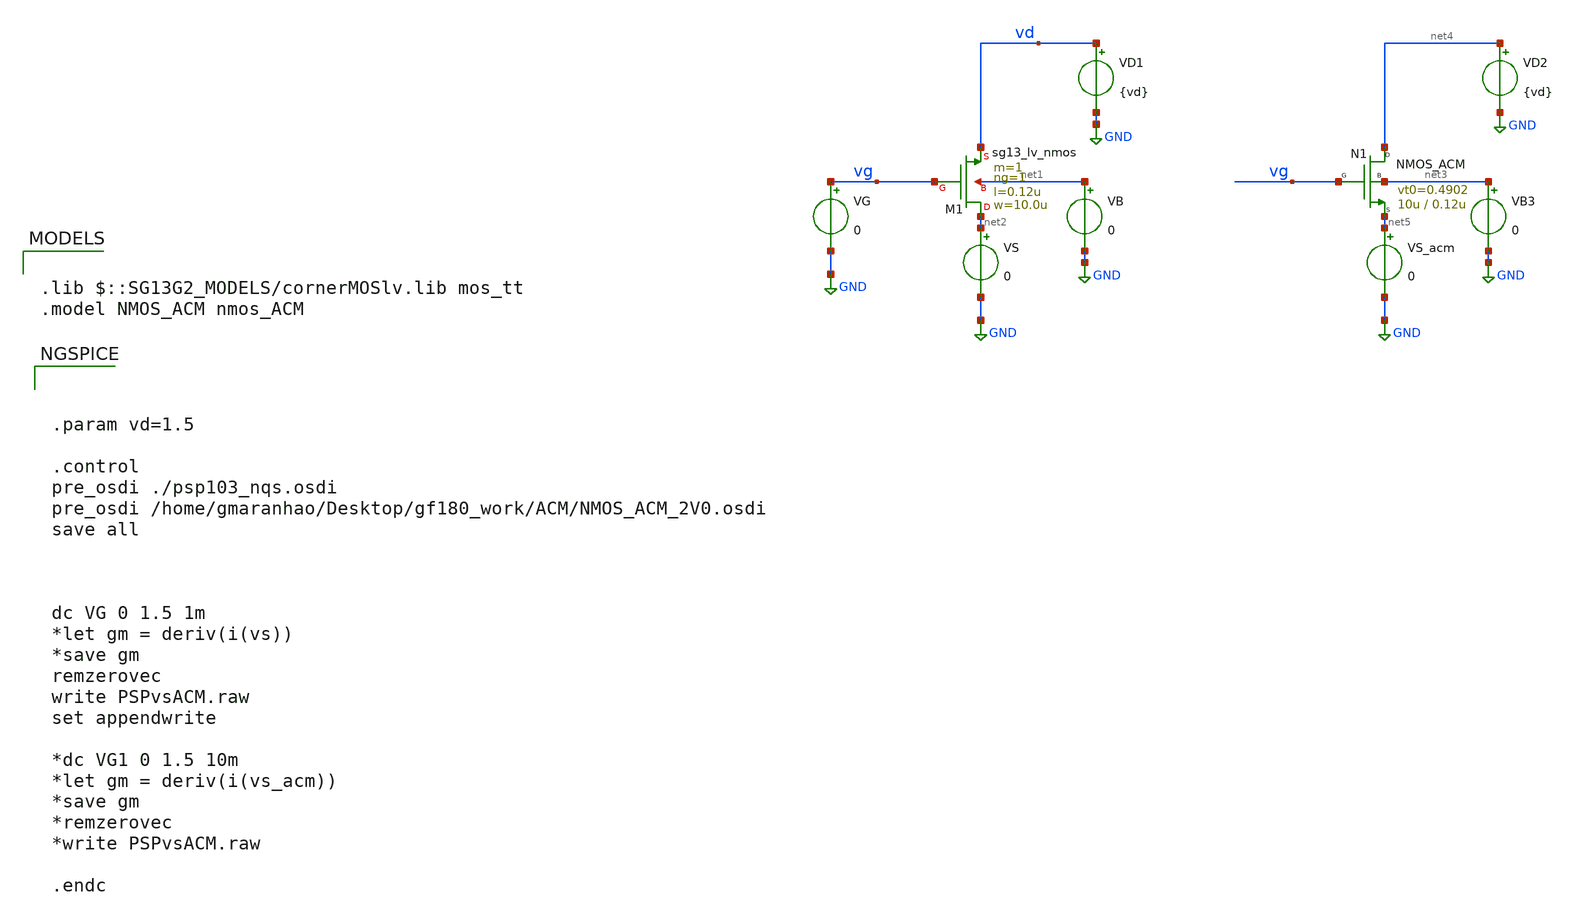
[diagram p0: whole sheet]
** sch_path: ihp_tutorials/PSPvsACM.sch
**.subckt PSPvsACM
VG vg GND 0
VD1 vd GND {vd}
VB net1 GND 0
VS net2 GND 0
N1 net4 vg net5 net3 NMOS_ACM w=10u l=0.12u n=1.414 is=11.77u vt0=0.4902 sigma=53.4m zeta=7m
VB3 net3 GND 0
VS_acm net5 GND 0
VD2 net4 GND {vd}
XM1 net2 vg vd net1 sg13_lv_nmos w=10.0u l=0.12u ng=1 m=1 mm_ok=1
**** begin user architecture code



.param vd=1.5

.control
pre_osdi ./psp103_nqs.osdi
pre_osdi /home/gmaranhao/Desktop/gf180_work/ACM/NMOS_ACM_2V0.osdi
save all



dc VG 0 1.5 1m
*let gm = deriv(i(vs))
*save gm
remzerovec
write PSPvsACM.raw
set appendwrite

*dc VG1 0 1.5 10m
*let gm = deriv(i(vs_acm))
*save gm
*remzerovec
*write PSPvsACM.raw

.endc



.lib $::SG13G2_MODELS/cornerMOSlv.lib mos_tt
.model NMOS_ACM nmos_ACM

**** end user architecture code
**.ends
.GLOBAL GND
.end
